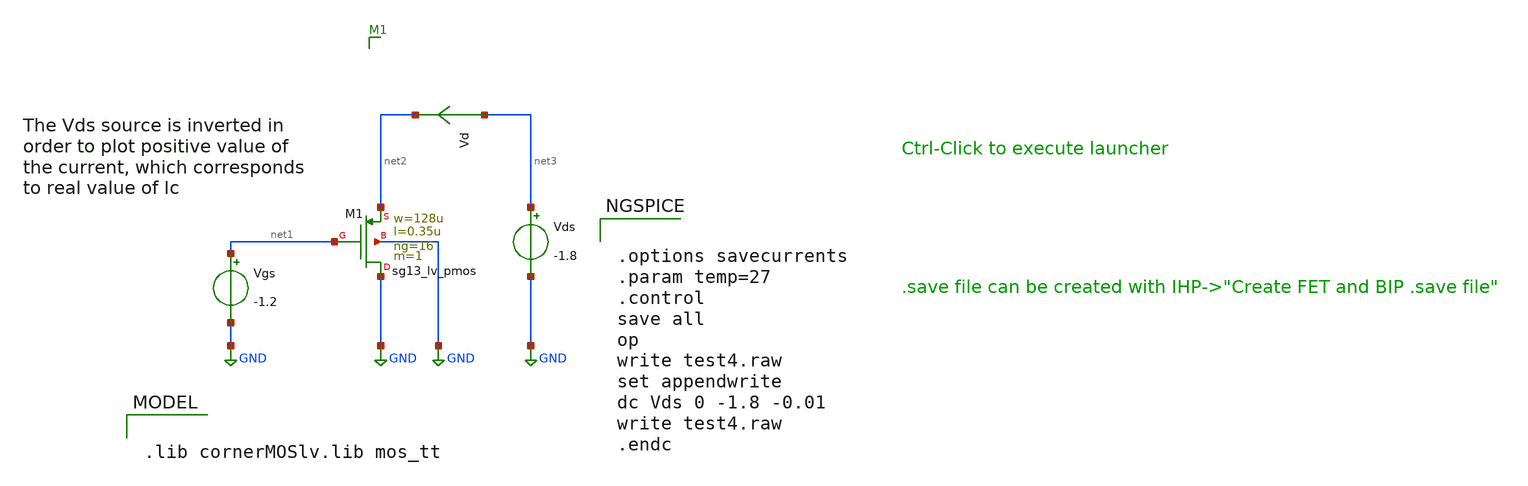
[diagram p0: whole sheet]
** sch_path: schematic/test4.sch
**.subckt test4
Vgs net1 GND -1.2
Vds net3 GND -1.8
Vd net3 net2 0
.save i(vd)
XM1 GND net1 net2 GND sg13_lv_pmos w=128u l=0.35u ng=16 m=1 mm_ok=1
**** begin user architecture code

.lib cornerMOSlv.lib mos_tt



.options savecurrents
.param temp=27
.control
save all
op
write test4.raw
set appendwrite
dc Vds 0 -1.8 -0.01
write test4.raw
.endc


**** end user architecture code
**.ends
.GLOBAL GND
.end
